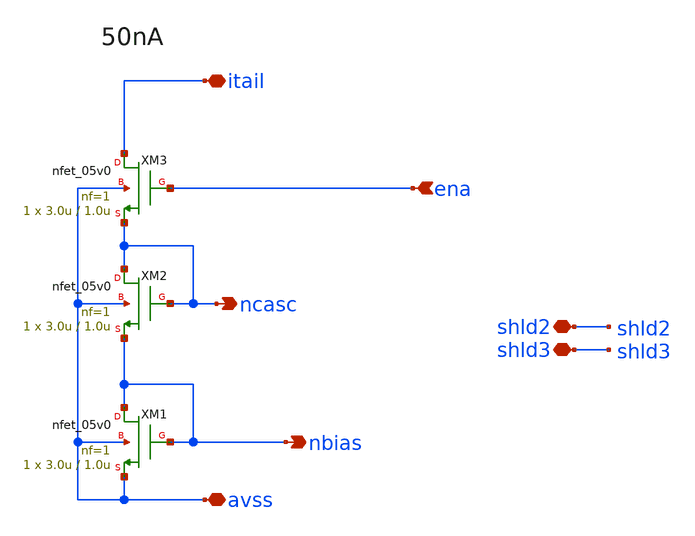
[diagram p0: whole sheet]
** sch_path: projects/programmable_transceiver_platform/analog/core_support/biasgen/xschem/bias_nset.sch
**.subckt bias_nset avss ena itail nbias ncasc shld2 shld3
*.iopin avss
*.ipin ena
*.iopin itail
*.opin nbias
*.opin ncasc
*.iopin shld2
*.iopin shld3
XM1 nbias nbias avss avss nfet_05v0 L=1.0u W=3.0u nf=1 ad='int((nf+1)/2) * W/nf * 0.18u' as='int((nf+2)/2) * W/nf * 0.18u'
+ pd='2*int((nf+1)/2) * (W/nf + 0.18u)' ps='2*int((nf+2)/2) * (W/nf + 0.18u)' nrd='0.18u / W' nrs='0.18u / W'
+ sa=0 sb=0 sd=0 m=1
XM2 ncasc ncasc nbias avss nfet_05v0 L=1.0u W=3.0u nf=1 ad='int((nf+1)/2) * W/nf * 0.18u' as='int((nf+2)/2) * W/nf * 0.18u'
+ pd='2*int((nf+1)/2) * (W/nf + 0.18u)' ps='2*int((nf+2)/2) * (W/nf + 0.18u)' nrd='0.18u / W' nrs='0.18u / W'
+ sa=0 sb=0 sd=0 m=1
XM3 itail ena ncasc avss nfet_05v0 L=1.0u W=3.0u nf=1 ad='int((nf+1)/2) * W/nf * 0.18u' as='int((nf+2)/2) * W/nf * 0.18u'
+ pd='2*int((nf+1)/2) * (W/nf + 0.18u)' ps='2*int((nf+2)/2) * (W/nf + 0.18u)' nrd='0.18u / W' nrs='0.18u / W'
+ sa=0 sb=0 sd=0 m=1
**.ends
.end
